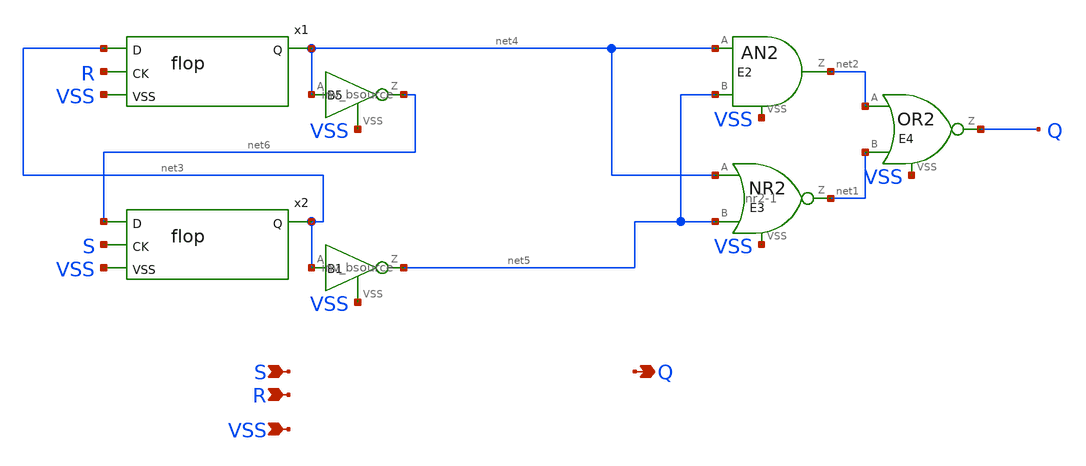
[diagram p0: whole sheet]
** sch_path: xschem-src/xschem_library/examples/sr_flop.sch
* Copyright (C) 1998-2026 Stefan Frederik Schippers
* This program is free software; you can redistribute it and/or modify
* it under the terms of the GNU General Public License as published by
* the Free Software Foundation; either version 2 of the License, or
* (at your option) any later version.
* This program is distributed in the hope that it will be useful,
* but WITHOUT ANY WARRANTY; without even the implied warranty of
* MERCHANTABILITY or FITNESS FOR A PARTICULAR PURPOSE.  See the
* GNU General Public License for more details.
* You should have received a copy of the GNU General Public License
* along with this program; if not, write to the Free Software
**.subckt sr_flop S Q VSS R
*.ipin S
*.opin Q
*.ipin VSS
*.ipin R
x1 net3 net4 R VSS flop VTH=VTH VHI=VHI
x2 net6 net3 S VSS flop VTH=VTH VHI=VHI
E2 net2 VSS and(2) net4 VSS net5 VSS 'VTH-0.1' 0.0 'VTH+0.1' VHI
E3 net1 VSS nor(2) net4 VSS net5 VSS 'VTH-0.1' VHI 'VTH+0.1' 0.0
E4 Q VSS or(2) net2 VSS net1 VSS 'VTH-0.1' 0.0 'VTH+0.1' VHI
B5 net6 VSS V=pwl(v( net4 , VSS ), 'VTH-0.1' VHI 'VTH+0.1' 0 )
B1 net5 VSS V=pwl(v( net3 , VSS ), 'VTH-0.1' VHI 'VTH+0.1' 0 )
**.ends

* expanding   symbol:  flop.sym # of pins=4
** sym_path: xschem-src/xschem_library/examples/flop.sym
** sch_path: xschem-src/xschem_library/examples/flop.sch
.subckt flop D Q CK VSS  VTH=1.5 VHI=3.0
*.ipin D
*.opin Q
*.ipin VSS
*.ipin CK
B5 net1 VSS V=pwl(v( CK , VSS ), 'VTH-0.1' VHI 'VTH+0.1' 0 )
x5 D net2 net1 VSS dlatch VTH=VTH VHI=VHI
x1 net2 Q CK VSS dlatch VTH=VTH VHI=VHI
.ends


* expanding   symbol:  dlatch.sym # of pins=4
** sym_path: xschem-src/xschem_library/examples/dlatch.sym
** sch_path: xschem-src/xschem_library/examples/dlatch.sch
.subckt dlatch D Q G VSS  VTH=1.5 VHI=3.0
*.ipin D
*.opin Q
*.ipin VSS
*.ipin G
G5 net2 net1 vcr pwl(1) G VSS 'VTH-0.1' 10G 'VTH+0.1' 10
c1 net2 VSS 1p m=1
E5 net1 VSS pwl(1) D VSS 'VTH-0.1' 0 'VTH+0.1' VHI
E1 Q VSS pwl(1) net2 VSS 'VTH-0.1' 0 'VTH+0.1' VHI
.ends

.end
